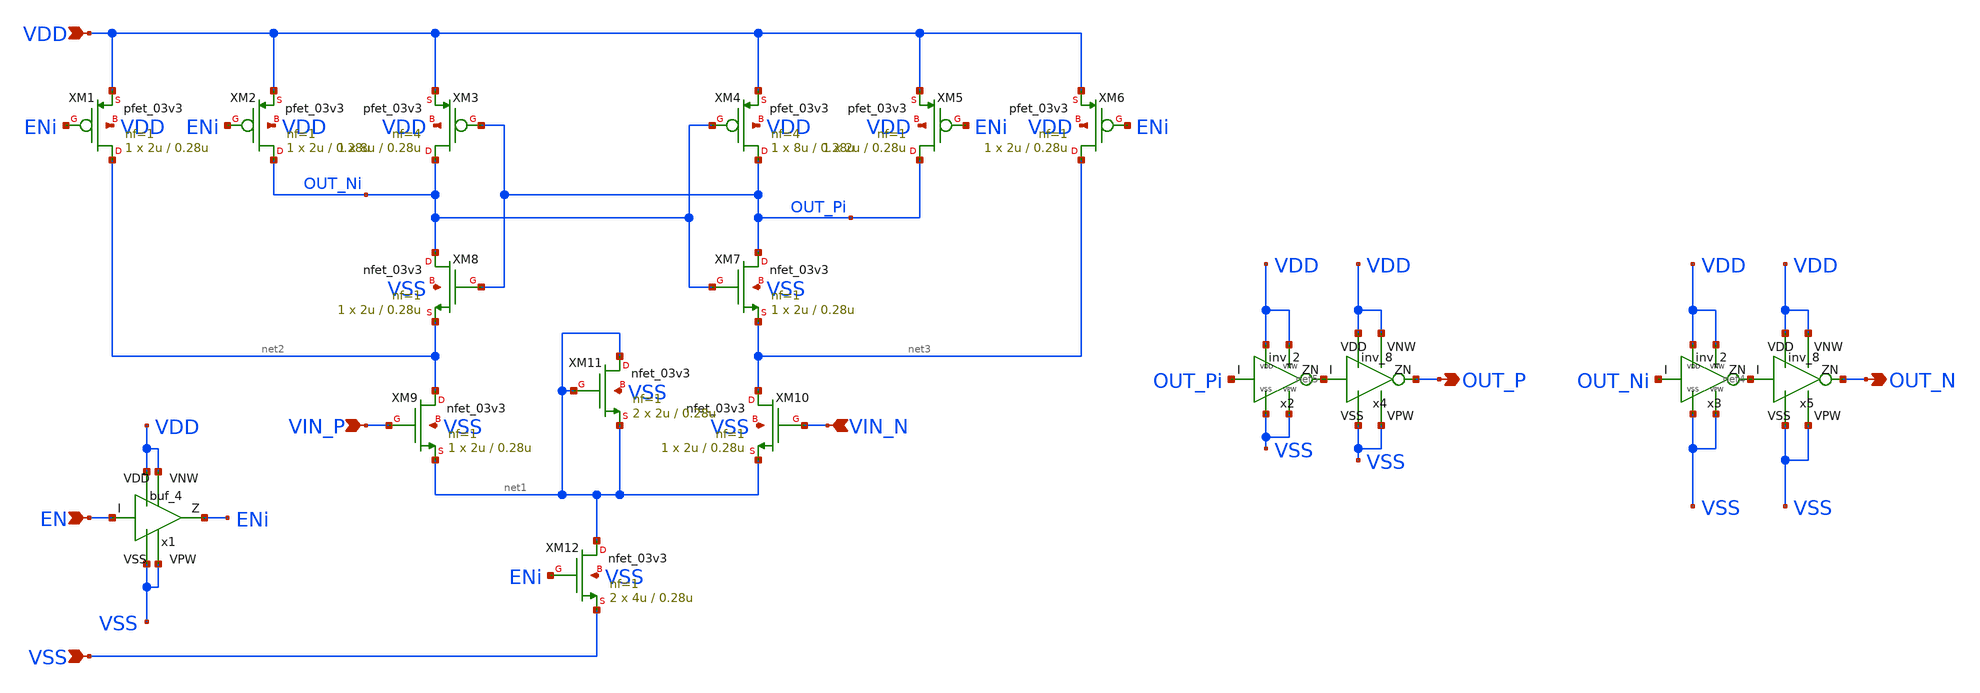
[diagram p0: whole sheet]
** sch_path: xschem/latched_comparator.sch
**.subckt latched_comparator VIN_P VIN_N VDD VSS EN OUT_N OUT_P
*.ipin VIN_P
*.ipin VIN_N
*.ipin VDD
*.ipin VSS
*.ipin EN
*.opin OUT_N
*.opin OUT_P
XM1 net2 ENi VDD VDD pfet_03v3 L=0.28u W=2u nf=1 ad='int((nf+1)/2) * W/nf * 0.18u' as='int((nf+2)/2) * W/nf * 0.18u'
+ pd='2*int((nf+1)/2) * (W/nf + 0.18u)' ps='2*int((nf+2)/2) * (W/nf + 0.18u)' nrd='0.18u / W' nrs='0.18u / W'
+ sa=0 sb=0 sd=0 m=1
XM2 OUT_Ni ENi VDD VDD pfet_03v3 L=0.28u W=2u nf=1 ad='int((nf+1)/2) * W/nf * 0.18u' as='int((nf+2)/2) * W/nf * 0.18u'
+ pd='2*int((nf+1)/2) * (W/nf + 0.18u)' ps='2*int((nf+2)/2) * (W/nf + 0.18u)' nrd='0.18u / W' nrs='0.18u / W'
+ sa=0 sb=0 sd=0 m=1
XM3 OUT_Ni OUT_Pi VDD VDD pfet_03v3 L=0.28u W=8u nf=4 ad='int((nf+1)/2) * W/nf * 0.18u' as='int((nf+2)/2) * W/nf * 0.18u'
+ pd='2*int((nf+1)/2) * (W/nf + 0.18u)' ps='2*int((nf+2)/2) * (W/nf + 0.18u)' nrd='0.18u / W' nrs='0.18u / W'
+ sa=0 sb=0 sd=0 m=1
XM4 OUT_Pi OUT_Ni VDD VDD pfet_03v3 L=0.28u W=8u nf=4 ad='int((nf+1)/2) * W/nf * 0.18u' as='int((nf+2)/2) * W/nf * 0.18u'
+ pd='2*int((nf+1)/2) * (W/nf + 0.18u)' ps='2*int((nf+2)/2) * (W/nf + 0.18u)' nrd='0.18u / W' nrs='0.18u / W'
+ sa=0 sb=0 sd=0 m=1
XM5 OUT_Pi ENi VDD VDD pfet_03v3 L=0.28u W=2u nf=1 ad='int((nf+1)/2) * W/nf * 0.18u' as='int((nf+2)/2) * W/nf * 0.18u'
+ pd='2*int((nf+1)/2) * (W/nf + 0.18u)' ps='2*int((nf+2)/2) * (W/nf + 0.18u)' nrd='0.18u / W' nrs='0.18u / W'
+ sa=0 sb=0 sd=0 m=1
XM6 net3 ENi VDD VDD pfet_03v3 L=0.28u W=2u nf=1 ad='int((nf+1)/2) * W/nf * 0.18u' as='int((nf+2)/2) * W/nf * 0.18u'
+ pd='2*int((nf+1)/2) * (W/nf + 0.18u)' ps='2*int((nf+2)/2) * (W/nf + 0.18u)' nrd='0.18u / W' nrs='0.18u / W'
+ sa=0 sb=0 sd=0 m=1
XM7 OUT_Pi OUT_Ni net3 VSS nfet_03v3 L=0.28u W=2u nf=1 ad='int((nf+1)/2) * W/nf * 0.18u' as='int((nf+2)/2) * W/nf * 0.18u'
+ pd='2*int((nf+1)/2) * (W/nf + 0.18u)' ps='2*int((nf+2)/2) * (W/nf + 0.18u)' nrd='0.18u / W' nrs='0.18u / W'
+ sa=0 sb=0 sd=0 m=1
XM8 OUT_Ni OUT_Pi net2 VSS nfet_03v3 L=0.28u W=2u nf=1 ad='int((nf+1)/2) * W/nf * 0.18u' as='int((nf+2)/2) * W/nf * 0.18u'
+ pd='2*int((nf+1)/2) * (W/nf + 0.18u)' ps='2*int((nf+2)/2) * (W/nf + 0.18u)' nrd='0.18u / W' nrs='0.18u / W'
+ sa=0 sb=0 sd=0 m=1
XM9 net2 VIN_P net1 VSS nfet_03v3 L=0.28u W=2u nf=1 ad='int((nf+1)/2) * W/nf * 0.18u' as='int((nf+2)/2) * W/nf * 0.18u'
+ pd='2*int((nf+1)/2) * (W/nf + 0.18u)' ps='2*int((nf+2)/2) * (W/nf + 0.18u)' nrd='0.18u / W' nrs='0.18u / W'
+ sa=0 sb=0 sd=0 m=1
XM10 net3 VIN_N net1 VSS nfet_03v3 L=0.28u W=2u nf=1 ad='int((nf+1)/2) * W/nf * 0.18u' as='int((nf+2)/2) * W/nf * 0.18u'
+ pd='2*int((nf+1)/2) * (W/nf + 0.18u)' ps='2*int((nf+2)/2) * (W/nf + 0.18u)' nrd='0.18u / W' nrs='0.18u / W'
+ sa=0 sb=0 sd=0 m=1
XM11 net1 net1 net1 VSS nfet_03v3 L=0.28u W=2u nf=1 ad='int((nf+1)/2) * W/nf * 0.18u' as='int((nf+2)/2) * W/nf * 0.18u'
+ pd='2*int((nf+1)/2) * (W/nf + 0.18u)' ps='2*int((nf+2)/2) * (W/nf + 0.18u)' nrd='0.18u / W' nrs='0.18u / W'
+ sa=0 sb=0 sd=0 m=2
XM12 net1 ENi VSS VSS nfet_03v3 L=0.28u W=4u nf=1 ad='int((nf+1)/2) * W/nf * 0.18u' as='int((nf+2)/2) * W/nf * 0.18u'
+ pd='2*int((nf+1)/2) * (W/nf + 0.18u)' ps='2*int((nf+2)/2) * (W/nf + 0.18u)' nrd='0.18u / W' nrs='0.18u / W'
+ sa=0 sb=0 sd=0 m=2
x5 net4 OUT_N VDD VDD VSS VSS gf180mcu_fd_sc_mcu7t5v0__inv_8
x3 OUT_Ni net4 VDD VDD VSS VSS gf180mcu_fd_sc_mcu7t5v0__inv_2
x2 OUT_Pi net5 VDD VDD VSS VSS gf180mcu_fd_sc_mcu7t5v0__inv_2
x4 net5 OUT_P VDD VDD VSS VSS gf180mcu_fd_sc_mcu7t5v0__inv_8
x1 EN ENi VDD VDD VSS VSS gf180mcu_fd_sc_mcu7t5v0__buf_4
**.ends
.end
